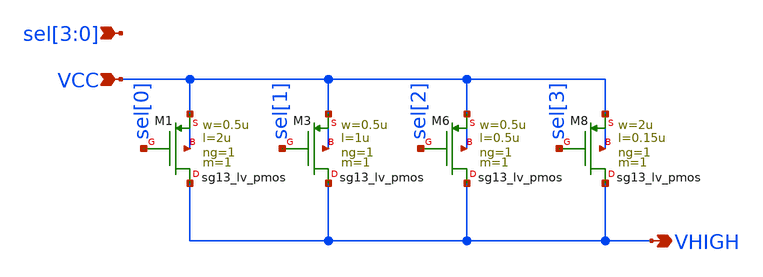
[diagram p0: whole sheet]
** sch_path: xschem/pmosbank.sch
**.subckt pmosbank VCC VHIGH sel[3],sel[2],sel[1],sel[0]
*.ipin VCC
*.opin VHIGH
*.ipin sel[3],sel[2],sel[1],sel[0]
XM1 VHIGH sel[0] VCC VCC sg13_lv_pmos w=0.5u l=2u ng=1 m=1 mm_ok=1
XM3 VHIGH sel[1] VCC VCC sg13_lv_pmos w=0.5u l=1u ng=1 m=1 mm_ok=1
XM6 VHIGH sel[2] VCC VCC sg13_lv_pmos w=0.5u l=0.5u ng=1 m=1 mm_ok=1
XM8 VHIGH sel[3] VCC VCC sg13_lv_pmos w=2u l=0.15u ng=1 m=1 mm_ok=1
**.ends
.end
